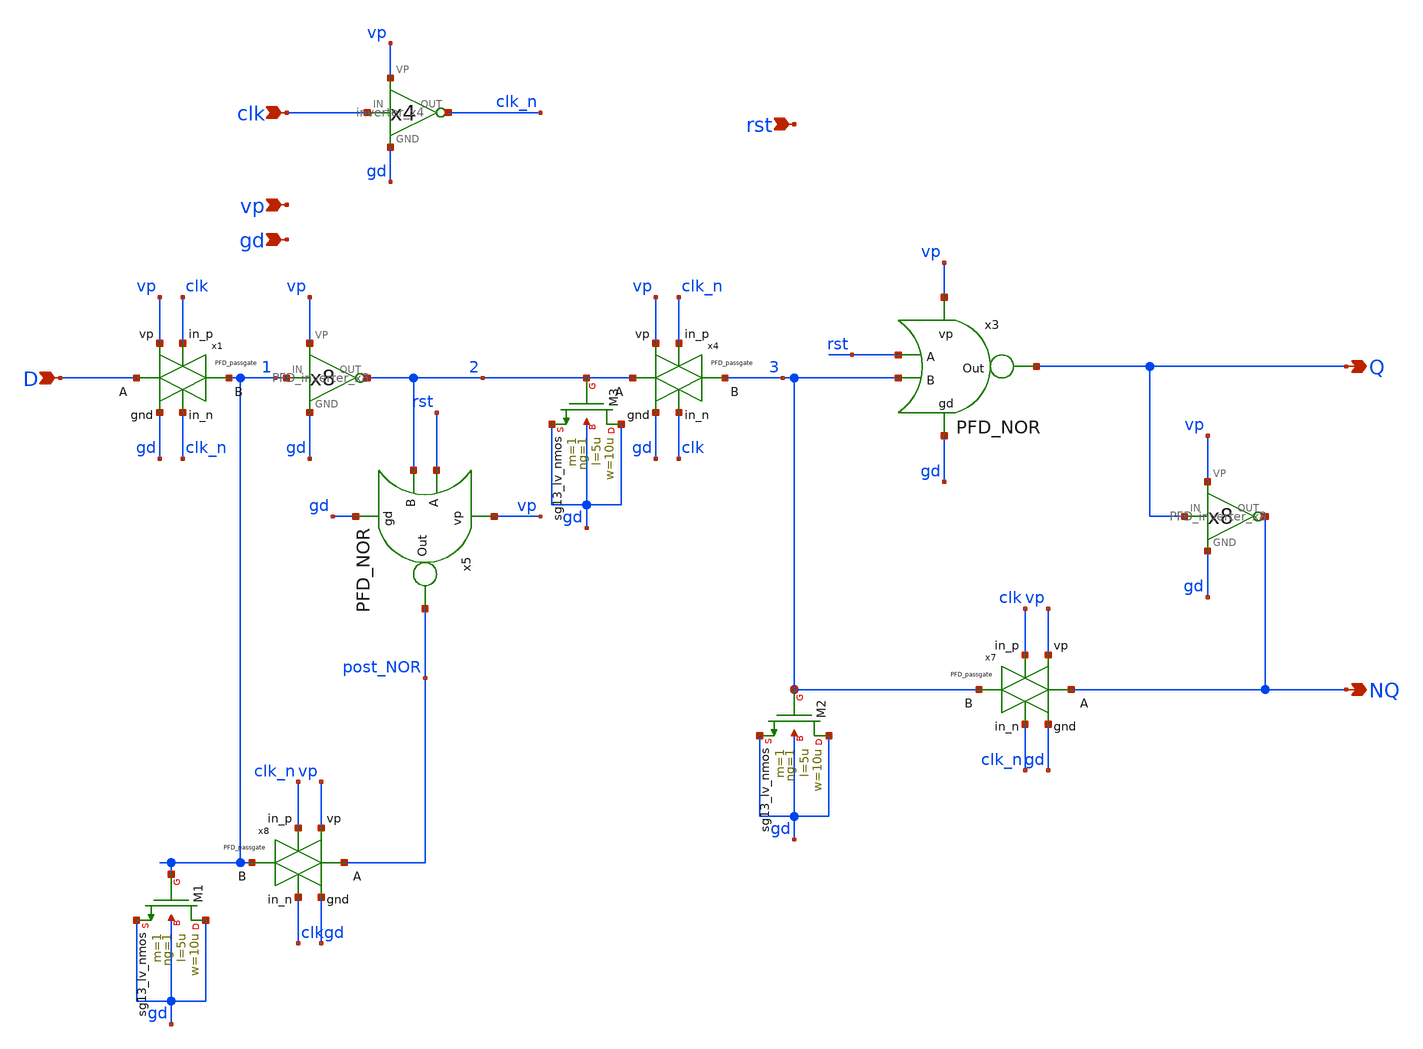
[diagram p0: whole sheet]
** sch_path: schematics/PFD/PFD_flip_flop.sch
**.subckt PFD_flip_flop D Q NQ clk rst gd vp
*.ipin D
*.opin Q
*.opin NQ
*.ipin clk
*.ipin rst
*.ipin gd
*.ipin vp
x8 clk vp post_NOR 1 gd clk_n PFD_passgate
x4 clk vp 2 3 gd clk_n PFD_passgate
x7 clk_n vp NQ 3 gd clk PFD_passgate
x3 vp rst 3 Q gd PFD_NOR
x5 vp rst 2 post_NOR gd PFD_NOR
x2 clk clk_n vp gd inverter_x4
x1 clk_n vp D 1 gd clk PFD_passgate
XM1 gd 1 gd gd sg13_lv_nmos w=10u l=5u ng=1 m=1 mm_ok=1
XM2 gd 3 gd gd sg13_lv_nmos w=10u l=5u ng=1 m=1 mm_ok=1
XM3 gd 2 gd gd sg13_lv_nmos w=10u l=5u ng=1 m=1 mm_ok=1
x9 1 2 vp gd PFD_inverter_x8
x6 Q NQ vp gd PFD_inverter_x8
**.ends
.end
